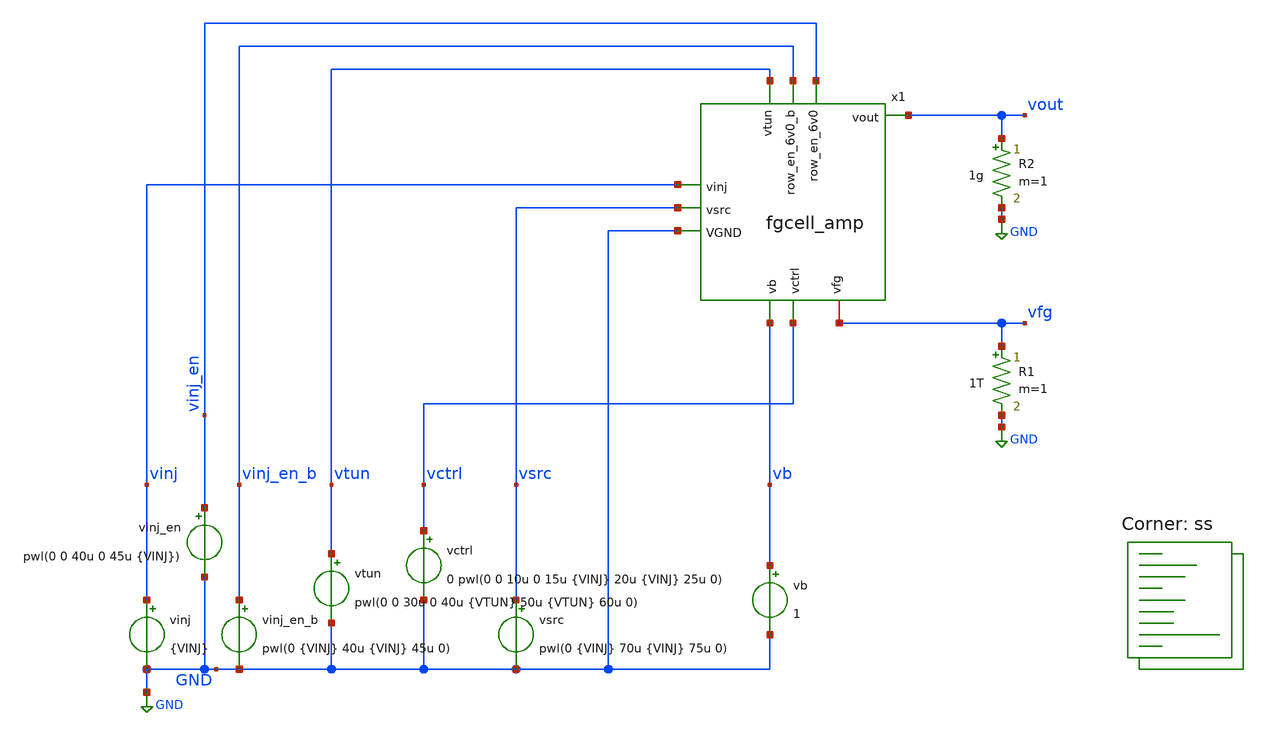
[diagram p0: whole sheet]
** sch_path: xschem/test_fgcell_amp.sch
**.subckt test_fgcell_amp
vinj_en_b vinj_en_b GND pwl(0 {VINJ} 40u {VINJ} 45u 0)
vctrl vctrl GND 0 pwl(0 0 10u 0 15u {VINJ} 20u {VINJ} 25u 0)
vsrc vsrc GND pwl(0 {VINJ} 70u {VINJ} 75u 0)
vtun vtun GND pwl(0 0 30u 0 40u {VTUN} 50u {VTUN} 60u 0)
vinj vinj GND {VINJ}
R1 vfg GND 1T m=1
x1 vfg vctrl vinj vinj_en_b vsrc vtun GND vout vinj_en vb fgcell_amp
vinj_en vinj_en GND pwl(0 0 40u 0 45u {VINJ})
vb vb GND 1
R2 vout GND 1g m=1
**** begin user architecture code
.lib $::SKYWATER_MODELS/sky130.lib.spice ss



.options reltol=0.0001 abstol=10e-15 chgtol=1e-15
.include fgcell.spice
.include diffamp_nmos.spice
.include tg5v0.spice
.param VTUN=12
.param VINJ=5
.param VDD=1.8
.param VSS=0
.option savecurrents
.ic v(vfg)=3
.control
  save all
  op
  remzerovec
  write test_fgcell_amp.raw
  set appendwrite
  tran 10n 120u uic
  remzerovec
  write test_fgcell_amp.raw
.endc



**** end user architecture code
**.ends

* expanding   symbol:  fgcell_amp.sym # of pins=10
** sym_path: xschem/fgcell_amp.sym
** sch_path: xschem/fgcell_amp.sch
.subckt fgcell_amp vfg vctrl vinj row_en_6v0_b vsrc vtun VGND vout row_en_6v0 vb
*.ipin vinj
*.ipin row_en_6v0_b
*.ipin vtun
*.ipin vctrl
*.ipin vsrc
*.ipin vb
*.ipin VGND
*.opin vout
*.iopin vfg
*.ipin row_en_6v0
x1 vinj row_en_6v0_b vtun vctrl vsrc VGND vfg fgcell
x2 vfg net1 vb net1 vinj VGND diffamp_nmos
x3 net1 vout row_en_6v0 row_en_6v0_b vinj VGND tg5v0
.ends

.GLOBAL GND
.end
